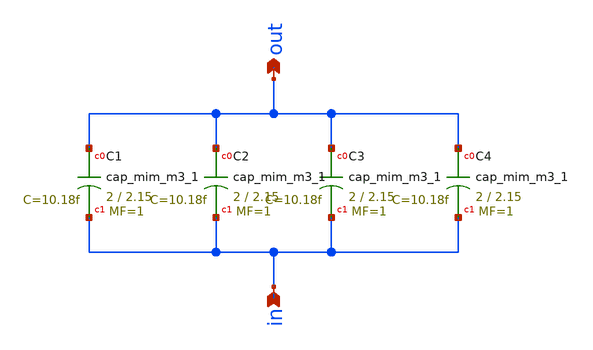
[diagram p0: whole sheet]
** sch_path: xschem/cap4.sch
**.subckt cap4 in out
*.ipin in
*.opin out
XC1 out in sky130_fd_pr__cap_mim_m3_1 W=2 L=2.15 MF=1 m=1
XC2 out in sky130_fd_pr__cap_mim_m3_1 W=2 L=2.15 MF=1 m=1
XC3 out in sky130_fd_pr__cap_mim_m3_1 W=2 L=2.15 MF=1 m=1
XC4 out in sky130_fd_pr__cap_mim_m3_1 W=2 L=2.15 MF=1 m=1
**.ends
.end
